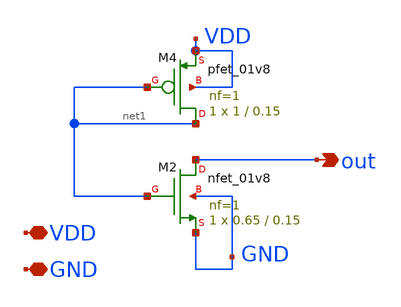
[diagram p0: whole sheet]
** sch_path: design/xschem/tie_low.sch
**.subckt tie_low VDD GND out
*.iopin VDD
*.iopin GND
*.opin out
XM4 net1 net1 VDD VDD sky130_fd_pr__pfet_01v8 L=0.15 W=1 nf=1 ad='int((nf+1)/2) * W/nf * 0.29' as='int((nf+2)/2) * W/nf * 0.29'
+ pd='2*int((nf+1)/2) * (W/nf + 0.29)' ps='2*int((nf+2)/2) * (W/nf + 0.29)' nrd='0.29 / W' nrs='0.29 / W'
+ sa=0 sb=0 sd=0 mult=1 m=1
XM2 out net1 GND GND sky130_fd_pr__nfet_01v8 L=0.15 W=0.65 nf=1 ad='int((nf+1)/2) * W/nf * 0.29' as='int((nf+2)/2) * W/nf * 0.29'
+ pd='2*int((nf+1)/2) * (W/nf + 0.29)' ps='2*int((nf+2)/2) * (W/nf + 0.29)' nrd='0.29 / W' nrs='0.29 / W'
+ sa=0 sb=0 sd=0 mult=1 m=1
**.ends
.end
